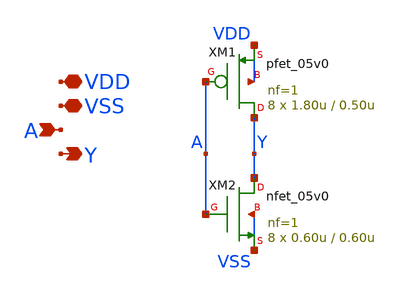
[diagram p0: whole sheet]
** sch_path: designs/libs/core_analog/switch-matrix/inv_8.sch
**.subckt inv_8 VDD VSS A Y
*.iopin VDD
*.iopin VSS
*.ipin A
*.opin Y
XM1 Y A VDD VDD pfet_05v0 L=0.50u W=1.80u nf=1 ad='int((nf+1)/2) * W/nf * 0.18u' as='int((nf+2)/2) * W/nf * 0.18u'
+ pd='2*int((nf+1)/2) * (W/nf + 0.18u)' ps='2*int((nf+2)/2) * (W/nf + 0.18u)' nrd='0.18u / W' nrs='0.18u / W'
+ sa=0 sb=0 sd=0 m=8
XM2 Y A VSS VSS nfet_05v0 L=0.60u W=0.60u nf=1 ad='int((nf+1)/2) * W/nf * 0.18u' as='int((nf+2)/2) * W/nf * 0.18u'
+ pd='2*int((nf+1)/2) * (W/nf + 0.18u)' ps='2*int((nf+2)/2) * (W/nf + 0.18u)' nrd='0.18u / W' nrs='0.18u / W'
+ sa=0 sb=0 sd=0 m=8
**.ends
.end
